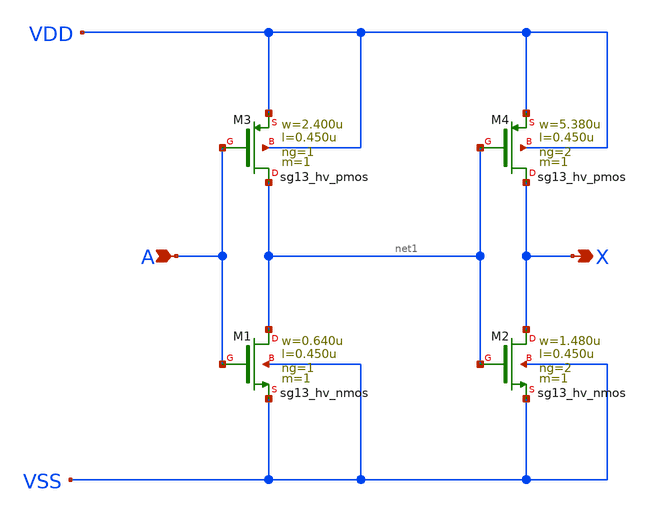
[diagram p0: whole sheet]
** sch_path: ihp-sg13g2/libs.ref/sg13g2_stdcell_hv/sch/xschem/sg13g2_hv_buf_2.sch
* Copyright 2023 IHP PDK Authors
* Licensed under the Apache License, Version 2.0 (the "License");
* you may not use this file except in compliance with the License.
* You may obtain a copy of the License at
* https://www.apache.org/licenses/LICENSE-2.0
* Unless required by applicable law or agreed to in writing, software
* distributed under the License is distributed on an "AS IS" BASIS,
* WITHOUT WARRANTIES OR CONDITIONS OF ANY KIND, either express or implied.
* See the License for the specific language governing permissions and
* limitations under the License.
**.subckt sg13g2_hv_buf_2 A X
*.ipin A
*.opin X
XM1 net1 A VSS VSS sg13_hv_nmos w=0.640u l=0.450u ng=1 m=1 mm_ok=1
XM2 X net1 VSS VSS sg13_hv_nmos w=1.480u l=0.450u ng=2 m=1 mm_ok=1
XM3 net1 A VDD VDD sg13_hv_pmos w=2.400u l=0.450u ng=1 m=1 mm_ok=1
XM4 X net1 VDD VDD sg13_hv_pmos w=5.380u l=0.450u ng=2 m=1 mm_ok=1
**.ends
.end
